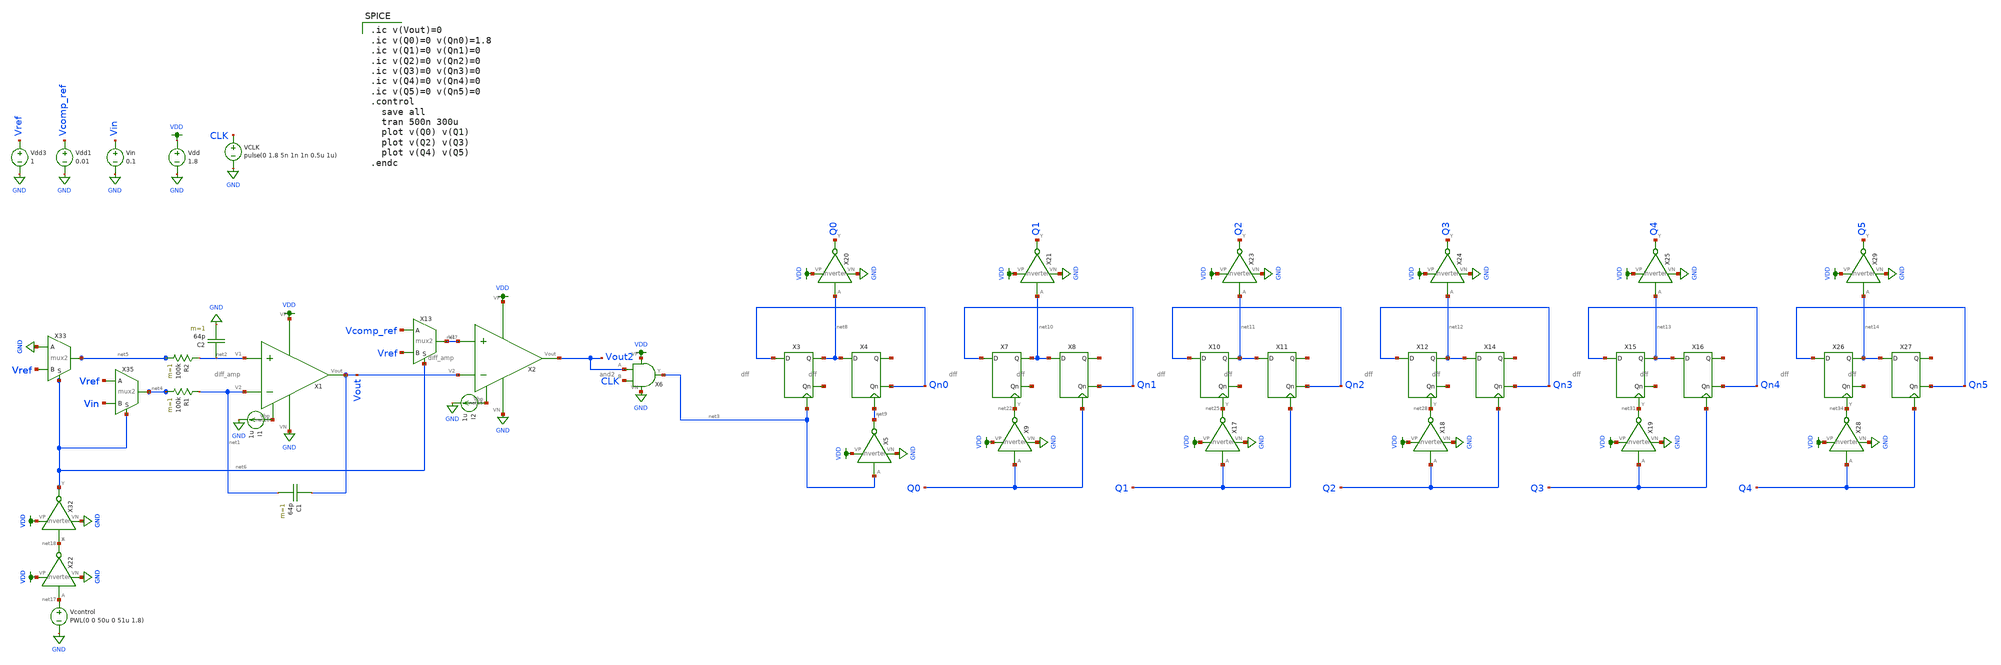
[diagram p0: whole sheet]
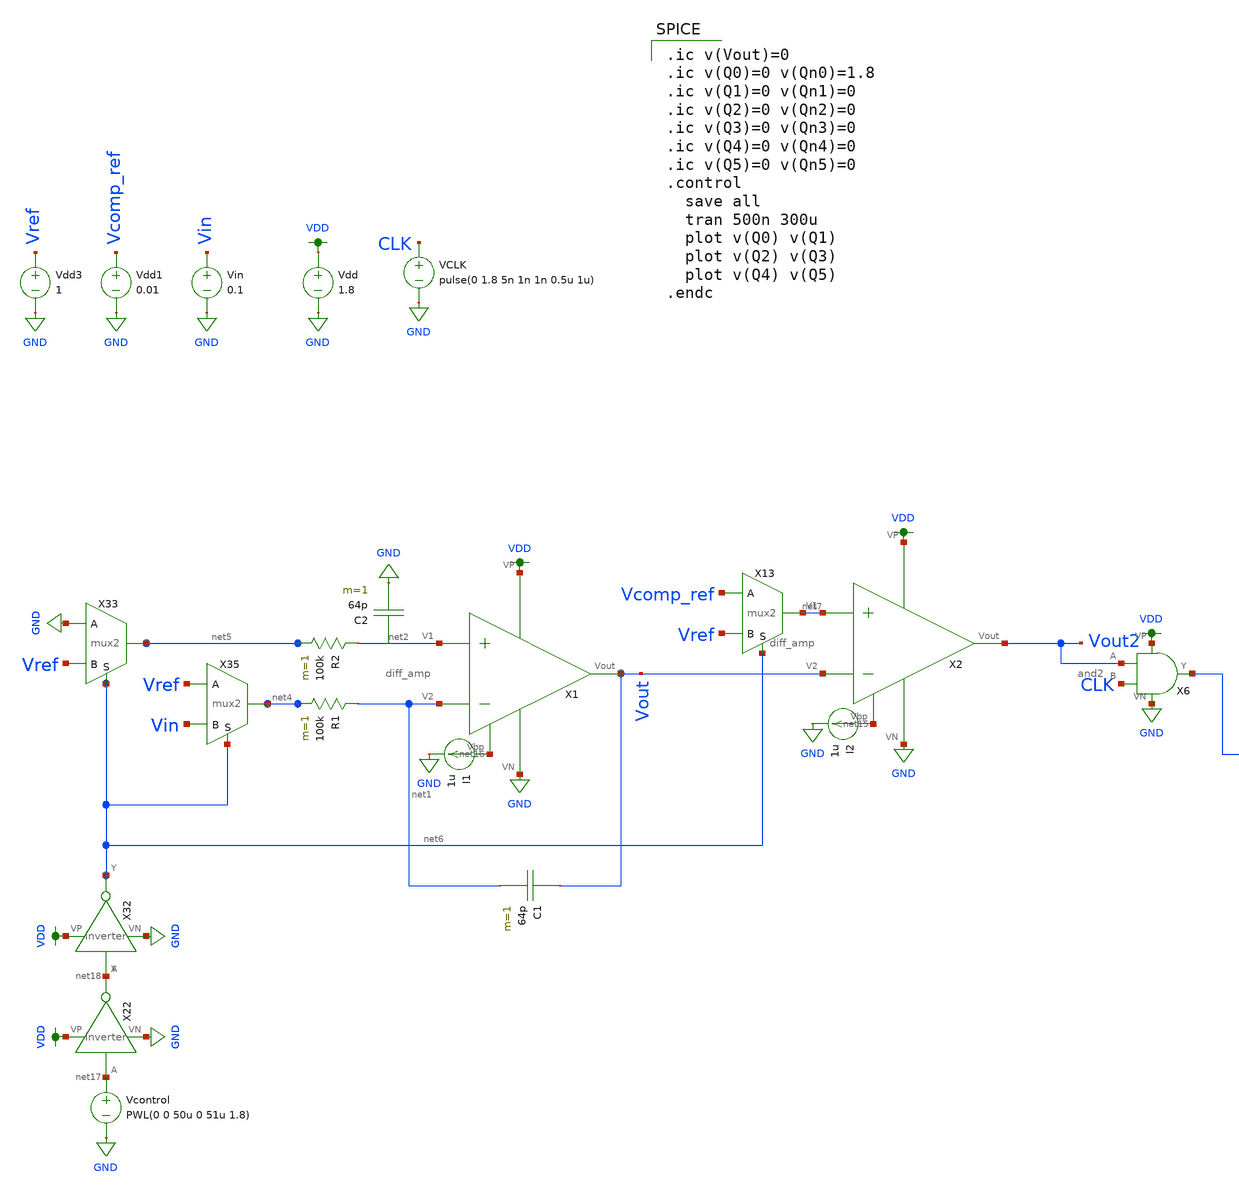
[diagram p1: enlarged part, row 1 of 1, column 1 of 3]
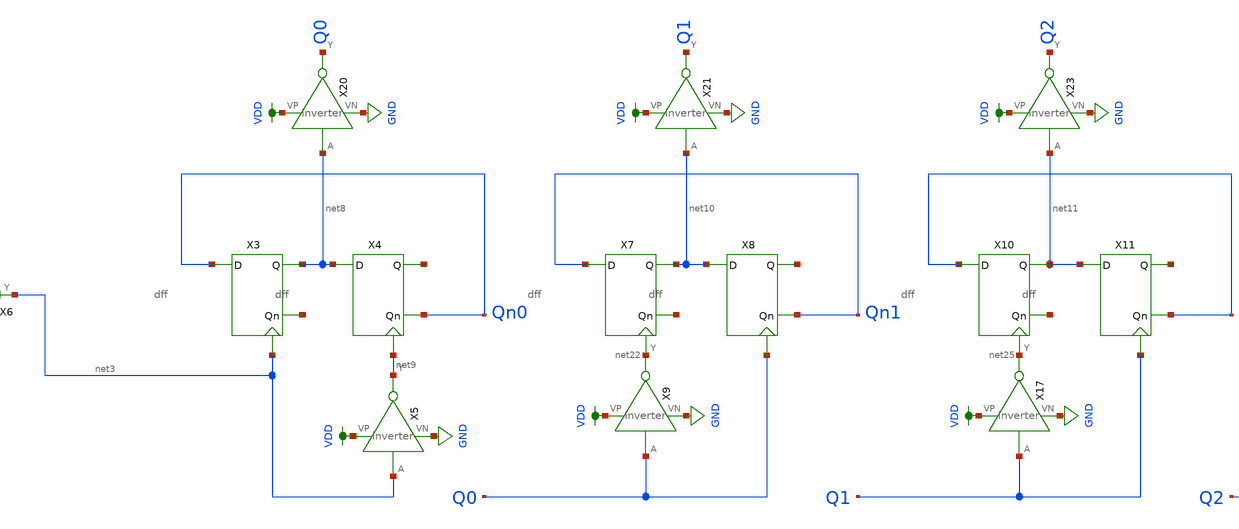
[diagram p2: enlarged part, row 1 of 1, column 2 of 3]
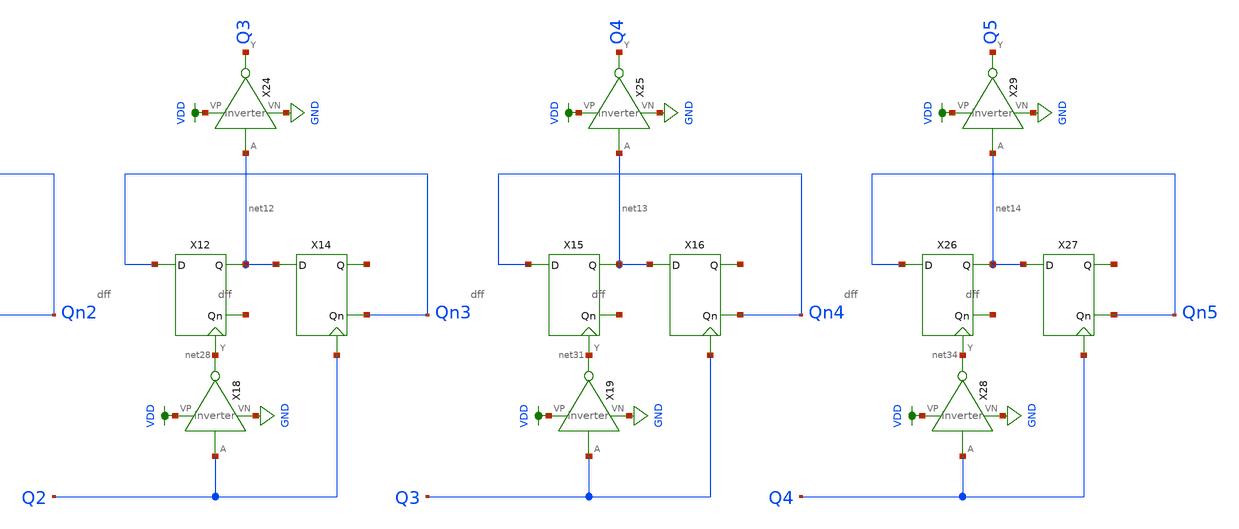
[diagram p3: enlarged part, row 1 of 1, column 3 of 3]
** sch_path: schematic/archive/double-slope-thomas_new.sch
**.subckt double-slope-thomas_new
X2 VDD net15 Vout2 net7 Vout GND diff_amp
Vdd VDD GND 1.8
VCLK CLK GND pulse(0 1.8 5n 1n 1n 0.5u 1u)
Vdd1 Vcomp_ref GND 0.01
Vin Vin GND 0.1
I2 net15 GND 1u
C1 Vout net1 64p m=1
X1 VDD net16 Vout net2 net1 GND diff_amp
R1 net1 net4 100k m=1
C2 net2 GND 64p m=1
R2 net2 net5 100k m=1
I1 net16 GND 1u
Vdd3 Vref GND 1
X6 VDD Vout2 GND net3 CLK and2
X13 net7 Vcomp_ref Vref net6 mux2
Vcontrol net17 GND PWL(0 0 50u 0 51u 1.8)
X22 net17 net18 VDD GND inverter
X32 net18 net6 VDD GND inverter
X33 net5 GND Vref net6 mux2
X35 net4 Vref Vin net6 mux2
X3 Qn0 net19 net8 net3 dff
X4 net8 Qn0 net20 net9 dff
X5 net3 net9 VDD GND inverter
X7 Qn1 net21 net10 net22 dff
X8 net10 Qn1 net23 Q0 dff
X9 Q0 net22 VDD GND inverter
X10 Qn2 net24 net11 net25 dff
X11 net11 Qn2 net26 Q1 dff
X12 Qn3 net27 net12 net28 dff
X14 net12 Qn3 net29 Q2 dff
X15 Qn4 net30 net13 net31 dff
X16 net13 Qn4 net32 Q3 dff
X17 Q1 net25 VDD GND inverter
X18 Q2 net28 VDD GND inverter
X19 Q3 net31 VDD GND inverter
X20 net8 Q0 VDD GND inverter
X21 net10 Q1 VDD GND inverter
X23 net11 Q2 VDD GND inverter
X24 net12 Q3 VDD GND inverter
X25 net13 Q4 VDD GND inverter
X26 Qn5 net33 net14 net34 dff
X27 net14 Qn5 net35 Q4 dff
X28 Q4 net34 VDD GND inverter
X29 net14 Q5 VDD GND inverter
**** begin user architecture code

.ic v(Vout)=0
.ic v(Q0)=0 v(Qn0)=1.8
.ic v(Q1)=0 v(Qn1)=0
.ic v(Q2)=0 v(Qn2)=0
.ic v(Q3)=0 v(Qn3)=0
.ic v(Q4)=0 v(Qn4)=0
.ic v(Q5)=0 v(Qn5)=0
.control
  save all
  tran 500n 300u
  plot v(Q0) v(Q1)
  plot v(Q2) v(Q3)
  plot v(Q4) v(Q5)
.endc


.option wnflag=1
.param MC_SWITCH=0.0
.lib ~/skywater/skywater-pdk/libraries/sky130_fd_pr_ngspice/latest/models/sky130.lib.spice tt

**** end user architecture code
**.ends
.GLOBAL GND
.GLOBAL VDD
.end
